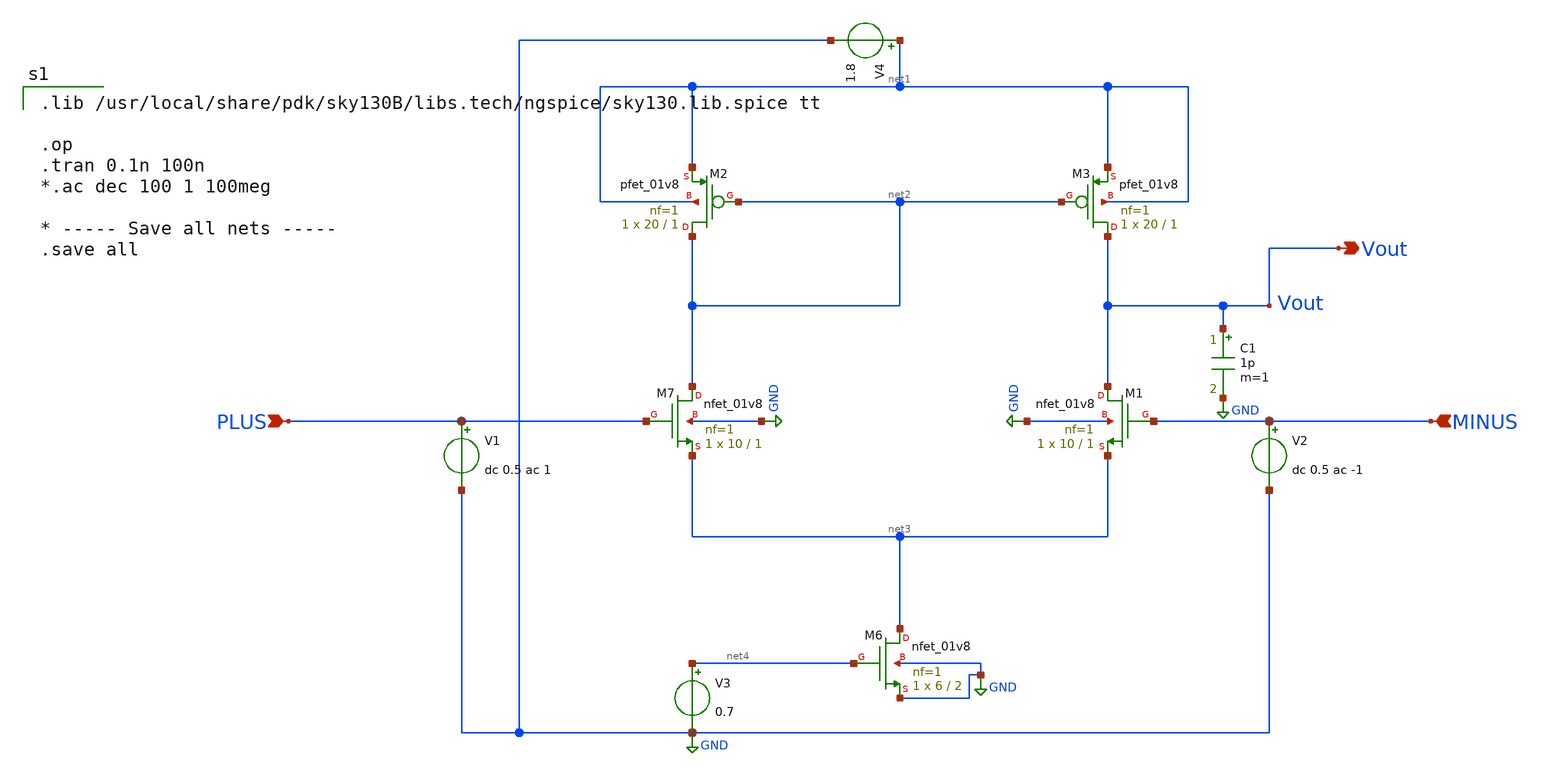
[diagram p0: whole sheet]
** sch_path: 5t-ota.sch
**.subckt 5t-ota MINUS PLUS Vout
*.ipin MINUS
*.ipin PLUS
*.opin Vout
C1 Vout GND 1p m=1
XM6 net3 net4 GND GND sky130_fd_pr__nfet_01v8 L=2 W=6 nf=1 ad=1.16u as=1.16u pd=8.58u ps=8.58u
+ nrd=0.0725 nrs=0.0725 sa=0 sb=0 sd=0 mult=1 m=1
XM7 net2 PLUS net3 GND sky130_fd_pr__nfet_01v8 L=1 W=10 nf=1 ad=1.16u as=1.16u pd=8.58u ps=8.58u
+ nrd=0.0725 nrs=0.0725 sa=0 sb=0 sd=0 mult=1 m=1
XM2 net2 net2 net1 net1 sky130_fd_pr__pfet_01v8 L=1 W=20 nf=1 ad=0.29u as=0.29u pd=2.58u ps=2.58u
+ nrd=0.29 nrs=0.29 sa=0 sb=0 sd=0 mult=1 m=1
XM3 Vout net2 net1 net1 sky130_fd_pr__pfet_01v8 L=1 W=20 nf=1 ad=0.29u as=0.29u pd=2.58u ps=2.58u
+ nrd=0.29 nrs=0.29 sa=0 sb=0 sd=0 mult=1 m=1
V3 net4 GND 0.7
XM1 Vout MINUS net3 GND sky130_fd_pr__nfet_01v8 L=1 W=10 nf=1 ad=1.16u as=1.16u pd=8.58u ps=8.58u
+ nrd=0.0725 nrs=0.0725 sa=0 sb=0 sd=0 mult=1 m=1
V1 PLUS GND dc 0.5 ac 1
V2 MINUS GND dc 0.5 ac -1
V4 net1 GND 1.8
**** begin user architecture code

.lib /usr/local/share/pdk/sky130B/libs.tech/ngspice/sky130.lib.spice tt

.op
.tran 0.1n 100n
*.ac dec 100 1 100meg

* ----- Save all nets -----
.save all


**** end user architecture code
**.ends
.GLOBAL GND
.end
